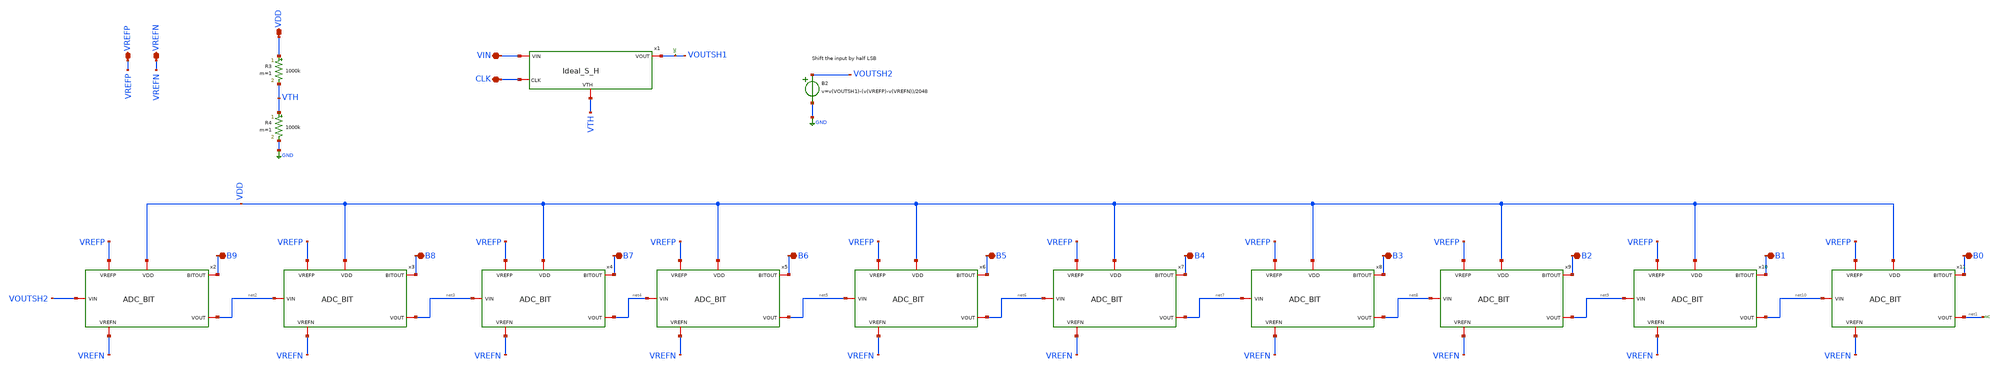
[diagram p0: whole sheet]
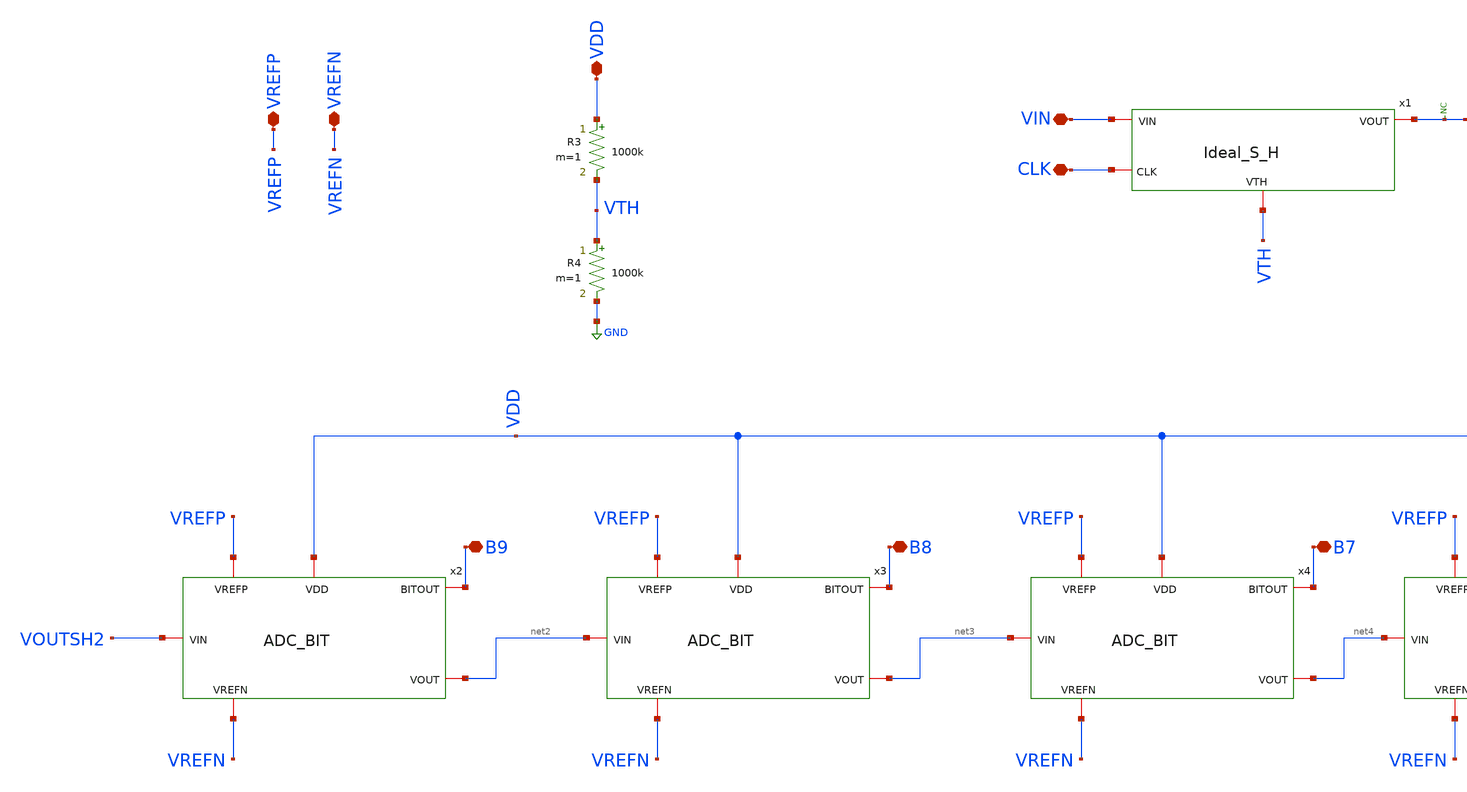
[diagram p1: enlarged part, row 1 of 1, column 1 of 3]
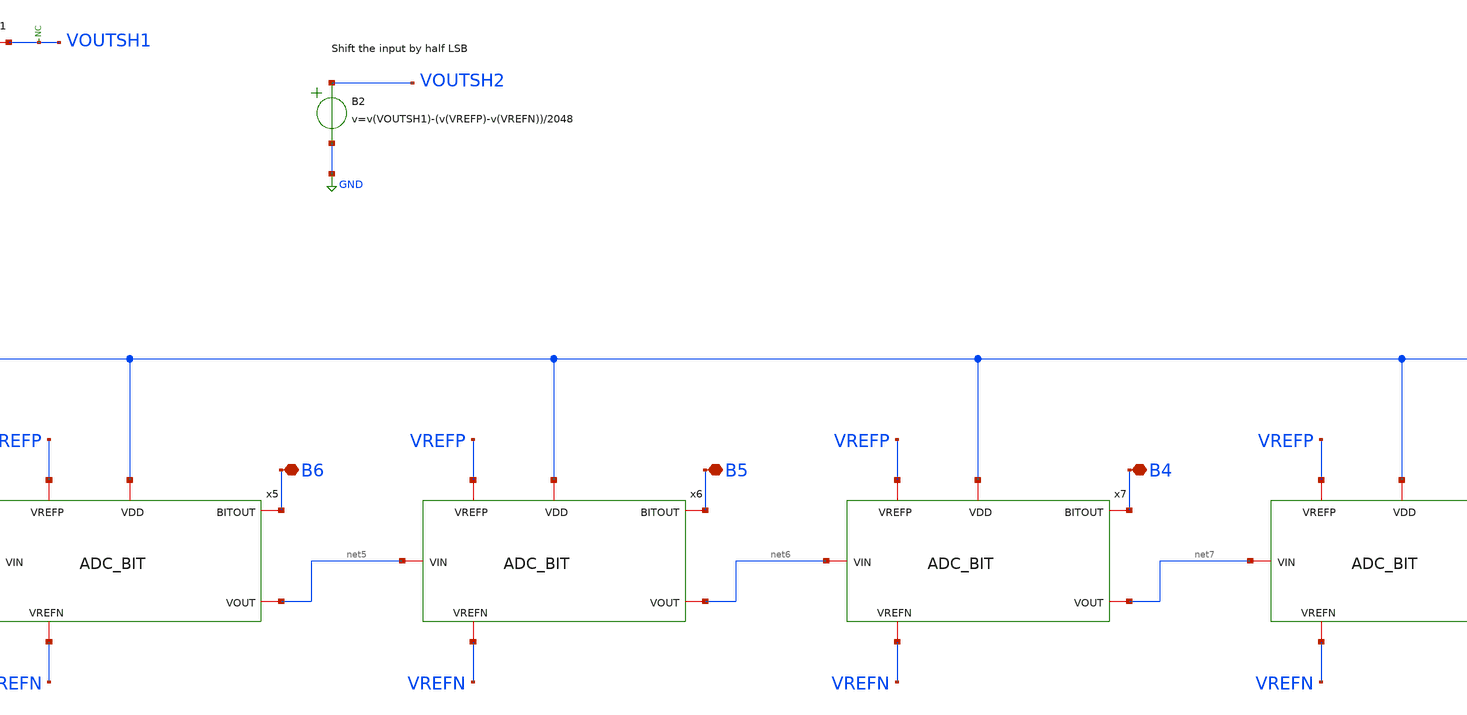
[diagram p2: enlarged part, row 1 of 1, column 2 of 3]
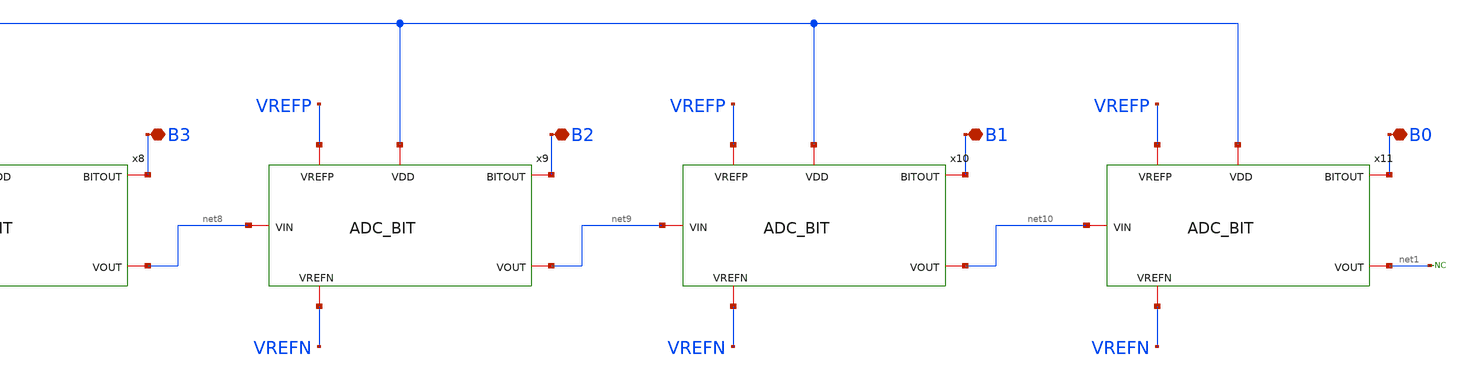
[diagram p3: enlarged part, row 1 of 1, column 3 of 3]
** sch_path: Designs/ADC_10.sch
**.subckt ADC_10 B9 B8 B7 B6 B5 B4 B3 B2 B1 B0 VDD VIN CLK VREFP VREFN
*.iopin B9
*.iopin B8
*.iopin B7
*.iopin B6
*.iopin B5
*.iopin B4
*.iopin B3
*.iopin B2
*.iopin B1
*.iopin B0
*.iopin VDD
*.iopin VIN
*.iopin CLK
*.iopin VREFP
*.iopin VREFN
x1 CLK VTH VOUTSH1 VIN Ideal_S_H
x2 VDD VREFN net2 VOUTSH2 B9 VREFP ADC_BIT
x3 VDD VREFN net3 net2 B8 VREFP ADC_BIT
x4 VDD VREFN net4 net3 B7 VREFP ADC_BIT
x5 VDD VREFN net5 net4 B6 VREFP ADC_BIT
x6 VDD VREFN net6 net5 B5 VREFP ADC_BIT
x7 VDD VREFN net7 net6 B4 VREFP ADC_BIT
x8 VDD VREFN net8 net7 B3 VREFP ADC_BIT
x9 VDD VREFN net9 net8 B2 VREFP ADC_BIT
x10 VDD VREFN net10 net9 B1 VREFP ADC_BIT
x11 VDD VREFN net1 net10 B0 VREFP ADC_BIT
* noconn #net1
B2 VOUTSH2 GND v=v(VOUTSH1)-(v(VREFP)-v(VREFN))/2048
R3 VDD VTH 1000k m=1
R4 VTH GND 1000k m=1
* noconn VOUTSH1
**.ends
.GLOBAL GND
.end
